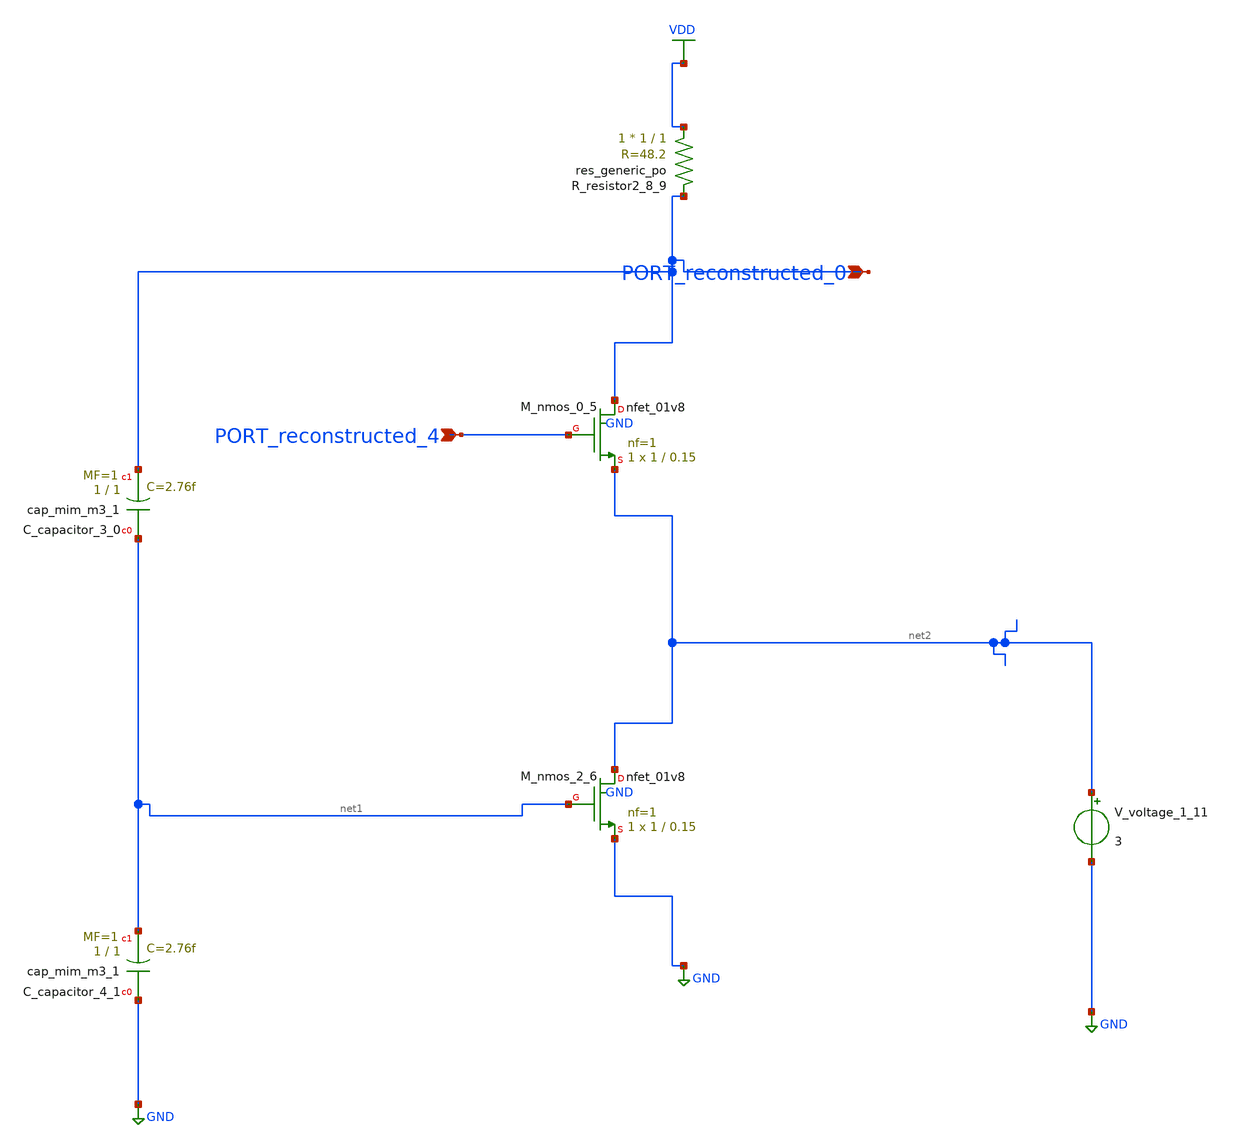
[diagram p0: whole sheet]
** sch_path: schematics/AMSNet/560.sch
**.subckt 560 PORT_reconstructed_0 PORT_reconstructed_4
*.ipin PORT_reconstructed_0
*.ipin PORT_reconstructed_4
XC_capacitor_3_0 net1 PORT_reconstructed_0 sky130_fd_pr__cap_mim_m3_1 W=1 L=1 MF=1 m=1
XC_capacitor_4_1 GND net1 sky130_fd_pr__cap_mim_m3_1 W=1 L=1 MF=1 m=1
XM_nmos_0_5 PORT_reconstructed_0 PORT_reconstructed_4 net2 GND sky130_fd_pr__nfet_01v8 L=0.15 W=1 nf=1
+ ad='int((1 + 1)/2) * 1 / 1 * 0.29' as='int((1 + 2)/2) * 1 / 1 * 0.29' pd='2*int((1 + 1)/2) * (1 / 1 + 0.29)'
+ ps='2*int((1 + 2)/2) * (1 / 1 + 0.29)' nrd='0.29 / 1 ' nrs='0.29 / 1 ' sa=0 sb=0 sd=0 mult=1 m=1
XM_nmos_2_6 net2 net1 GND GND sky130_fd_pr__nfet_01v8 L=0.15 W=1 nf=1 ad='int((1 + 1)/2) * 1 / 1 * 0.29'
+ as='int((1 + 2)/2) * 1 / 1 * 0.29' pd='2*int((1 + 1)/2) * (1 / 1 + 0.29)' ps='2*int((1 + 2)/2) * (1 / 1 + 0.29)'
+ nrd='0.29 / 1 ' nrs='0.29 / 1 ' sa=0 sb=0 sd=0 mult=1 m=1
XR_resistor2_8_9 VDD PORT_reconstructed_0 sky130_fd_pr__res_generic_po W=1 L=1 m=1
V_voltage_1_11 net2 GND 3
**.ends
.GLOBAL GND
.GLOBAL VDD
.end
